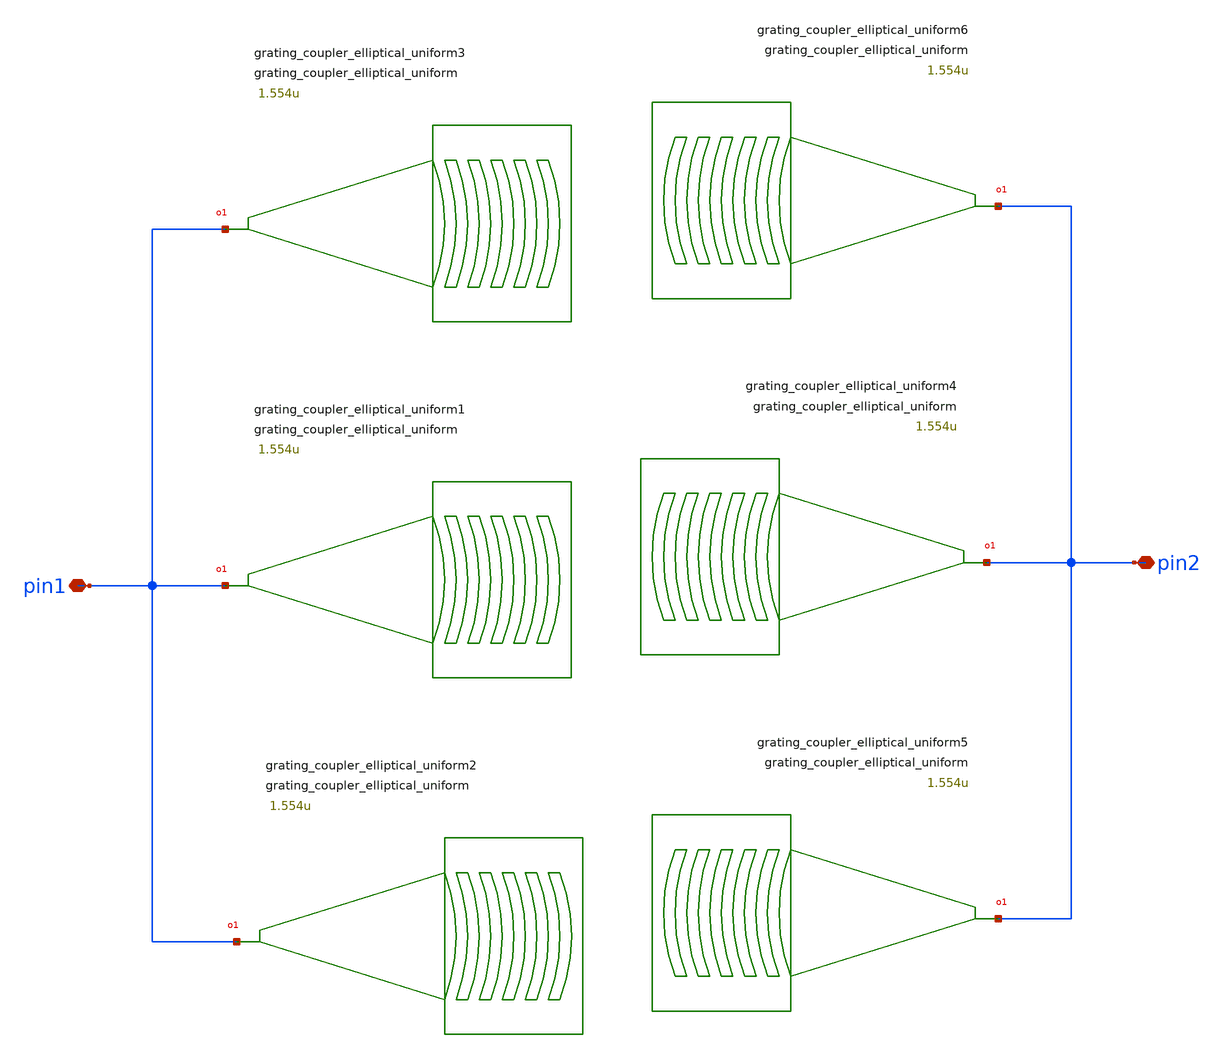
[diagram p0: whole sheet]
** sch_path: xschem/tests/test_sch/test_grating_coupler_elliptical_uniform.sch
* Copyright (c) 2024, Mabrains LLC
* Licensed under the GNU Lesser General Public License, Version 3.0 (the "License");
* you may not use this file except in compliance with the License.
* GNU Lesser General Public License
* Version 3, 29 June 2007
* This program is free software: you can redistribute it and/or modify
* it under the terms of the GNU Lesser General Public License as published
* by the Free Software Foundation, either version 3 of the License, or
* (at your option) any later version.
* This program is distributed in the hope that it will be useful,
* but WITHOUT ANY WARRANTY; without even the implied warranty of
* MERCHANTABILITY or FITNESS FOR A PARTICULAR PURPOSE.  See the
* GNU Lesser General Public License for more details.
* You should have received a copy of the GNU Lesser General Public License
* along with this program.  If not, see <https://www.gnu.org/licenses/>.
* SPDX-License-Identifier: LGPL-3.0
**.subckt test_grating_coupler_elliptical_uniform pin1 pin2
*.iopin pin1
*.iopin pin2
Pgrating_coupler_elliptical_uniform1 pin1 grating_coupler_elliptical_uniform n_periods=20
+ period=0.75 fill_factor=0.5 taper_length=16.6u taper_angle=60.0 wavelength=1.554u fiber_angle=15.0
+ taper_to_slab_offset=-3.0u bias_gap=0.0u
Pgrating_coupler_elliptical_uniform2 pin1 grating_coupler_elliptical_uniform n_periods=20
+ period=0.75 fill_factor=0.5 taper_length=16.6u taper_angle=60.0 wavelength=1.554u fiber_angle=15.0
+ taper_to_slab_offset=-3.0u bias_gap=0.0u
Pgrating_coupler_elliptical_uniform3 pin1 grating_coupler_elliptical_uniform n_periods=20
+ period=0.75 fill_factor=0.5 taper_length=16.6u taper_angle=60.0 wavelength=1.554u fiber_angle=15.0
+ taper_to_slab_offset=-3.0u bias_gap=0.0u
Pgrating_coupler_elliptical_uniform4 pin2 grating_coupler_elliptical_uniform n_periods=20
+ period=0.75 fill_factor=0.5 taper_length=16.6u taper_angle=60.0 wavelength=1.554u fiber_angle=15.0
+ taper_to_slab_offset=-3.0u bias_gap=0.0u
Pgrating_coupler_elliptical_uniform5 pin2 grating_coupler_elliptical_uniform n_periods=20
+ period=0.75 fill_factor=0.5 taper_length=16.6u taper_angle=60.0 wavelength=1.554u fiber_angle=15.0
+ taper_to_slab_offset=-3.0u bias_gap=0.0u
Pgrating_coupler_elliptical_uniform6 pin2 grating_coupler_elliptical_uniform n_periods=20
+ period=0.75 fill_factor=0.5 taper_length=16.6u taper_angle=60.0 wavelength=1.554u fiber_angle=15.0
+ taper_to_slab_offset=-3.0u bias_gap=0.0u
**.ends
.end
